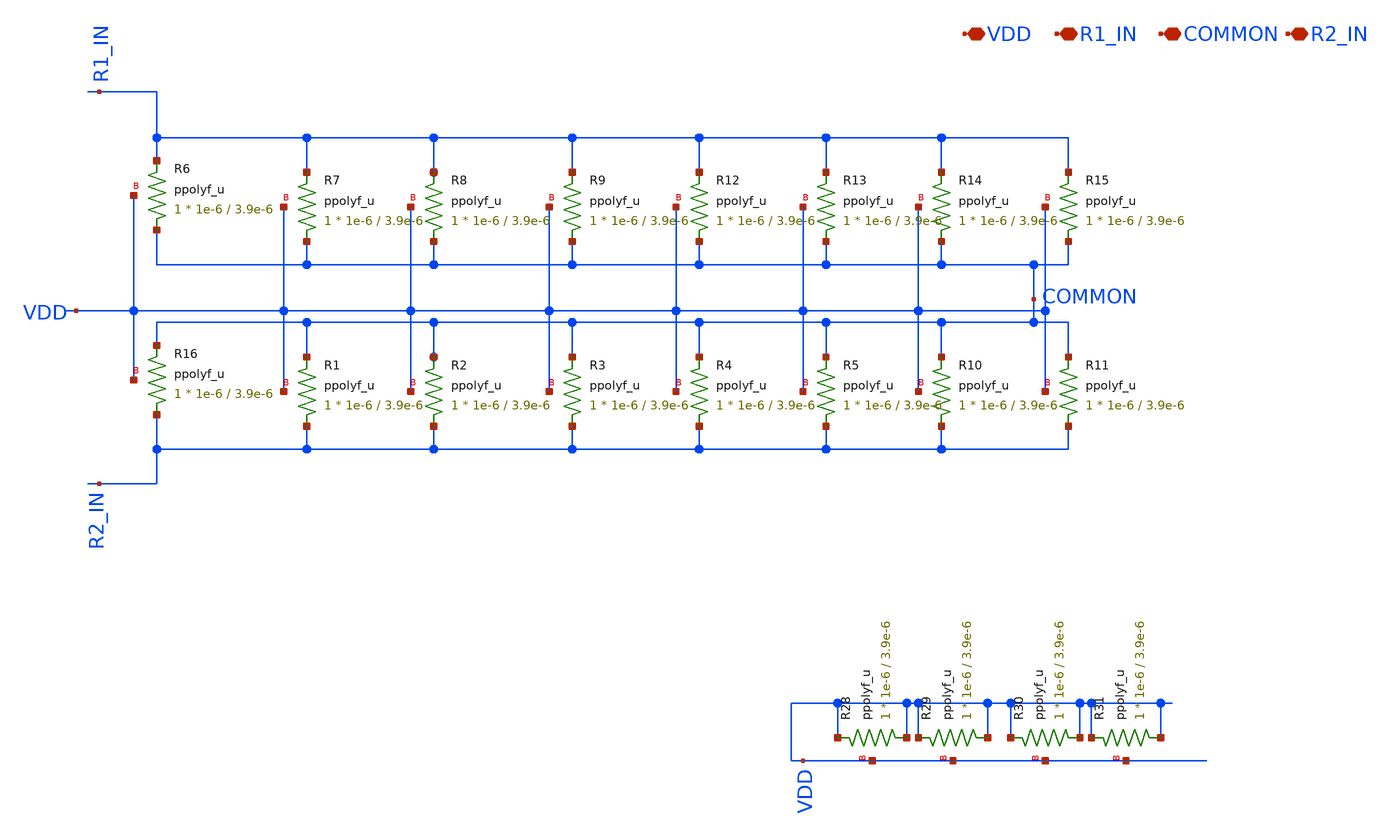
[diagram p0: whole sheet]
** sch_path: AWG_OUTPUT_AND_MUX_PAKISTAN_05/xschem/200_OHM.sch
**.subckt 200_OHM VDD R1_IN COMMON R2_IN
*.iopin VDD
*.iopin R1_IN
*.iopin COMMON
*.iopin R2_IN
XR28 VDD VDD VDD ppolyf_u r_width=1e-6 r_length=3.9e-6 m=1
XR29 VDD VDD VDD ppolyf_u r_width=1e-6 r_length=3.9e-6 m=1
XR30 VDD VDD VDD ppolyf_u r_width=1e-6 r_length=3.9e-6 m=1
XR31 VDD VDD VDD ppolyf_u r_width=1e-6 r_length=3.9e-6 m=1
XR6 COMMON R1_IN VDD ppolyf_u r_width=1e-6 r_length=3.9e-6 m=1
XR7 COMMON R1_IN VDD ppolyf_u r_width=1e-6 r_length=3.9e-6 m=1
XR8 COMMON R1_IN VDD ppolyf_u r_width=1e-6 r_length=3.9e-6 m=1
XR9 COMMON R1_IN VDD ppolyf_u r_width=1e-6 r_length=3.9e-6 m=1
XR12 COMMON R1_IN VDD ppolyf_u r_width=1e-6 r_length=3.9e-6 m=1
XR13 COMMON R1_IN VDD ppolyf_u r_width=1e-6 r_length=3.9e-6 m=1
XR14 COMMON R1_IN VDD ppolyf_u r_width=1e-6 r_length=3.9e-6 m=1
XR15 COMMON R1_IN VDD ppolyf_u r_width=1e-6 r_length=3.9e-6 m=1
XR1 R2_IN COMMON VDD ppolyf_u r_width=1e-6 r_length=3.9e-6 m=1
XR2 R2_IN COMMON VDD ppolyf_u r_width=1e-6 r_length=3.9e-6 m=1
XR3 R2_IN COMMON VDD ppolyf_u r_width=1e-6 r_length=3.9e-6 m=1
XR4 R2_IN COMMON VDD ppolyf_u r_width=1e-6 r_length=3.9e-6 m=1
XR5 R2_IN COMMON VDD ppolyf_u r_width=1e-6 r_length=3.9e-6 m=1
XR10 R2_IN COMMON VDD ppolyf_u r_width=1e-6 r_length=3.9e-6 m=1
XR11 R2_IN COMMON VDD ppolyf_u r_width=1e-6 r_length=3.9e-6 m=1
XR16 R2_IN COMMON VDD ppolyf_u r_width=1e-6 r_length=3.9e-6 m=1
**.ends
.end
